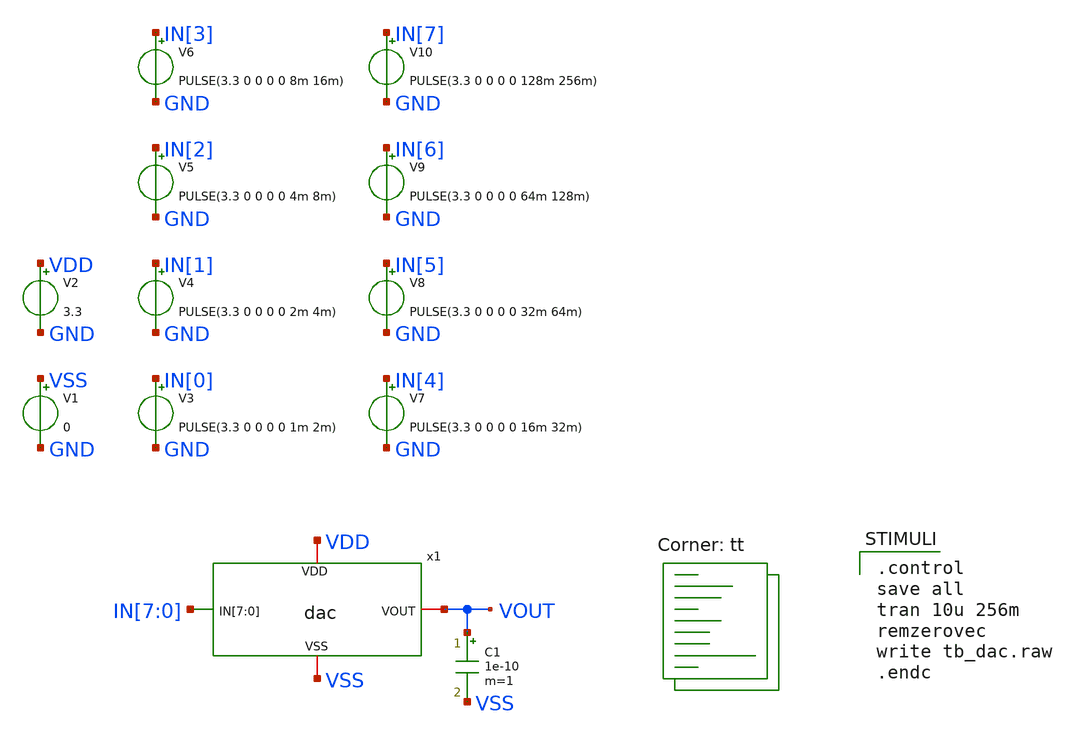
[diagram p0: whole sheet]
** sch_path: xschem/tb_dac.sch
**.subckt tb_dac
V1 VSS GND 0
V2 VDD GND 3.3
V3 IN[0] GND PULSE(3.3 0 0 0 0 1m 2m)
V4 IN[1] GND PULSE(3.3 0 0 0 0 2m 4m)
V5 IN[2] GND PULSE(3.3 0 0 0 0 4m 8m)
V6 IN[3] GND PULSE(3.3 0 0 0 0 8m 16m)
V7 IN[4] GND PULSE(3.3 0 0 0 0 16m 32m)
V8 IN[5] GND PULSE(3.3 0 0 0 0 32m 64m)
V9 IN[6] GND PULSE(3.3 0 0 0 0 64m 128m)
V10 IN[7] GND PULSE(3.3 0 0 0 0 128m 256m)
x1 VDD IN[7] IN[6] IN[5] IN[4] IN[3] IN[2] IN[1] IN[0] VOUT VSS dac
C1 VOUT VSS 1e-10 m=1
**** begin user architecture code
.lib $::SKYWATER_MODELS/sky130.lib.spice tt

.control
save all
tran 10u 256m
remzerovec
write tb_dac.raw
.endc

**** end user architecture code
**.ends
.end
